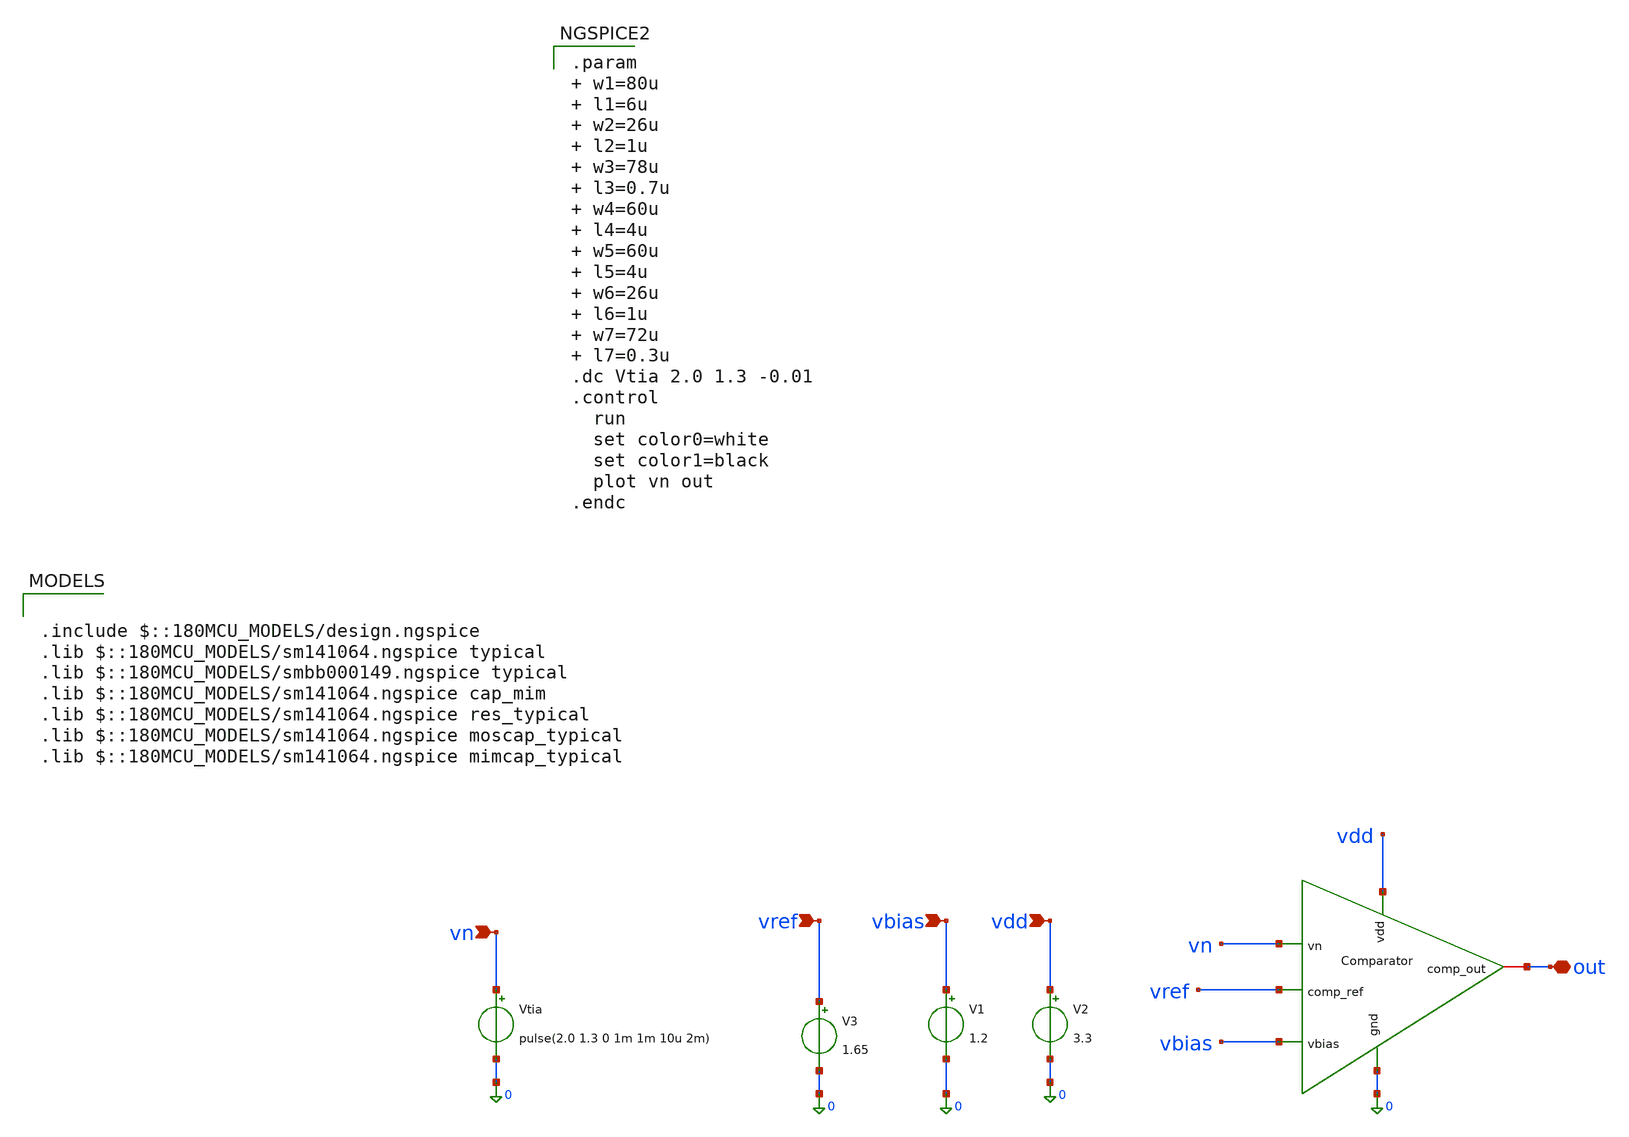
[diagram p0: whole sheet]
** sch_path: xschem/comparator/comp_tb.sch
**.subckt comp_tb out vbias vdd vref vn
*.iopin out
*.ipin vbias
*.ipin vdd
*.ipin vref
*.ipin vn
V1 vbias 0 1.2
V2 vdd 0 3.3
V3 vref 0 1.65
Vtia vn 0 pulse(2.0 1.3 0 1m 1m 10u 2m)
x2 vdd vn vref vbias 0 out comp
**** begin user architecture code

.include $::180MCU_MODELS/design.ngspice
.lib $::180MCU_MODELS/sm141064.ngspice typical
.lib $::180MCU_MODELS/smbb000149.ngspice typical
.lib $::180MCU_MODELS/sm141064.ngspice cap_mim
.lib $::180MCU_MODELS/sm141064.ngspice res_typical
.lib $::180MCU_MODELS/sm141064.ngspice moscap_typical
.lib $::180MCU_MODELS/sm141064.ngspice mimcap_typical


.param  w1=80u       l1=6u  w2=26u       l2=1u  w3=78u     l3=0.7u  w4=60u       l4=4u  w5=60u
+      l5=4u  w6=26u       l6=1u  w7=72u    l7=0.3u
.dc Vtia 2.0 1.3 -0.01
.control
  run
  set color0=white
  set color1=black
  plot vn out
.endc


**** end user architecture code
**.ends

* expanding   symbol:  GF180/xschem/Chipathon/Comparator/comp.sym # of pins=6
** sym_path: xschem/comparator/comp.sym
** sch_path: xschem/comparator/comp.sch
.subckt comp vdd vn comp_ref vbias gnd comp_out
*.ipin vn
*.ipin vbias
*.ipin vdd
*.ipin comp_ref
*.iopin comp_out
*.ipin gnd
XM1 net2 net1 gnd gnd nfet_03v3 L=0.28u W=0.22u nf=1 ad='int((nf+1)/2) * W/nf * 0.18u' as='int((nf+2)/2) * W/nf * 0.18u'
+ pd='2*int((nf+1)/2) * (W/nf + 0.18u)' ps='2*int((nf+2)/2) * (W/nf + 0.18u)' nrd='0.18u / W' nrs='0.18u / W'
+ sa=0 sb=0 sd=0 m=1
XM2 net2 net1 vdd vdd pfet_03v3 L=0.28u W=0.22u nf=1 ad='int((nf+1)/2) * W/nf * 0.18u' as='int((nf+2)/2) * W/nf * 0.18u'
+ pd='2*int((nf+1)/2) * (W/nf + 0.18u)' ps='2*int((nf+2)/2) * (W/nf + 0.18u)' nrd='0.18u / W' nrs='0.18u / W'
+ sa=0 sb=0 sd=0 m=1
XM5 comp_out net2 gnd gnd nfet_03v3 L=0.28u W=0.22u nf=1 ad='int((nf+1)/2) * W/nf * 0.18u' as='int((nf+2)/2) * W/nf * 0.18u'
+ pd='2*int((nf+1)/2) * (W/nf + 0.18u)' ps='2*int((nf+2)/2) * (W/nf + 0.18u)' nrd='0.18u / W' nrs='0.18u / W'
+ sa=0 sb=0 sd=0 m=1
XM6 comp_out net2 vdd vdd pfet_03v3 L=0.28u W=0.22u nf=1 ad='int((nf+1)/2) * W/nf * 0.18u' as='int((nf+2)/2) * W/nf * 0.18u'
+ pd='2*int((nf+1)/2) * (W/nf + 0.18u)' ps='2*int((nf+2)/2) * (W/nf + 0.18u)' nrd='0.18u / W' nrs='0.18u / W'
+ sa=0 sb=0 sd=0 m=1
x1 vdd vn gnd net1 net3 vbias opamp_poly
XR3 net3 comp_ref gnd ppolyf_u_1k r_width=1e-6 r_length=20e-6 m=1
XR1 net1 net3 gnd ppolyf_u_1k r_width=1e-6 r_length=500e-6 m=1
.ends


* expanding   symbol:  GF180/xschem/Chipathon/OpAMP_Silicon/opamp_poly.sym # of pins=6
** sym_path: OpAmP/opamp_poly.sym
** sch_path: OpAmP/opamp_poly.sch
.subckt opamp_poly vdd vn gnd out vp vbias
*.ipin gnd
*.iopin out
*.ipin vbias
*.ipin vp
*.ipin vn
*.ipin vdd
XM1 net3 vbias gnd gnd nfet_03v3 L=l1 W=w1 nf=1 ad='int((nf+1)/2) * W/nf * 0.18u' as='int((nf+2)/2) * W/nf * 0.18u'
+ pd='2*int((nf+1)/2) * (W/nf + 0.18u)' ps='2*int((nf+2)/2) * (W/nf + 0.18u)' nrd='0.18u / W' nrs='0.18u / W'
+ sa=0 sb=0 sd=0 m=1
XM2 net2 net2 vdd vdd pfet_03v3 L=l2 W=w2 nf=1 ad='int((nf+1)/2) * W/nf * 0.18u' as='int((nf+2)/2) * W/nf * 0.18u'
+ pd='2*int((nf+1)/2) * (W/nf + 0.18u)' ps='2*int((nf+2)/2) * (W/nf + 0.18u)' nrd='0.18u / W' nrs='0.18u / W'
+ sa=0 sb=0 sd=0 m=1
XM3 out vbias gnd gnd nfet_03v3 L=l3 W=w3 nf=1 ad='int((nf+1)/2) * W/nf * 0.18u' as='int((nf+2)/2) * W/nf * 0.18u'
+ pd='2*int((nf+1)/2) * (W/nf + 0.18u)' ps='2*int((nf+2)/2) * (W/nf + 0.18u)' nrd='0.18u / W' nrs='0.18u / W'
+ sa=0 sb=0 sd=0 m=1
XM4 net2 vn net3 gnd nfet_03v3 L=l4 W=w4 nf=1 ad='int((nf+1)/2) * W/nf * 0.18u' as='int((nf+2)/2) * W/nf * 0.18u'
+ pd='2*int((nf+1)/2) * (W/nf + 0.18u)' ps='2*int((nf+2)/2) * (W/nf + 0.18u)' nrd='0.18u / W' nrs='0.18u / W'
+ sa=0 sb=0 sd=0 m=1
XM5 net1 vp net3 gnd nfet_03v3 L=l5 W=w5 nf=1 ad='int((nf+1)/2) * W/nf * 0.18u' as='int((nf+2)/2) * W/nf * 0.18u'
+ pd='2*int((nf+1)/2) * (W/nf + 0.18u)' ps='2*int((nf+2)/2) * (W/nf + 0.18u)' nrd='0.18u / W' nrs='0.18u / W'
+ sa=0 sb=0 sd=0 m=1
XM6 net1 net2 vdd vdd pfet_03v3 L=l6 W=w6 nf=1 ad='int((nf+1)/2) * W/nf * 0.18u' as='int((nf+2)/2) * W/nf * 0.18u'
+ pd='2*int((nf+1)/2) * (W/nf + 0.18u)' ps='2*int((nf+2)/2) * (W/nf + 0.18u)' nrd='0.18u / W' nrs='0.18u / W'
+ sa=0 sb=0 sd=0 m=1
XM7 out net1 vdd vdd pfet_03v3 L=l7 W=w7 nf=1 ad='int((nf+1)/2) * W/nf * 0.18u' as='int((nf+2)/2) * W/nf * 0.18u'
+ pd='2*int((nf+1)/2) * (W/nf + 0.18u)' ps='2*int((nf+2)/2) * (W/nf + 0.18u)' nrd='0.18u / W' nrs='0.18u / W'
+ sa=0 sb=0 sd=0 m=1
XR1 net4 net1 gnd ppolyf_u_1k r_width=3e-6 r_length=6.6e-6 m=1
XC1 out net4 cap_mim_1f5fF c_width=20e-6 c_length=20e-6 m=1
.ends

.end
